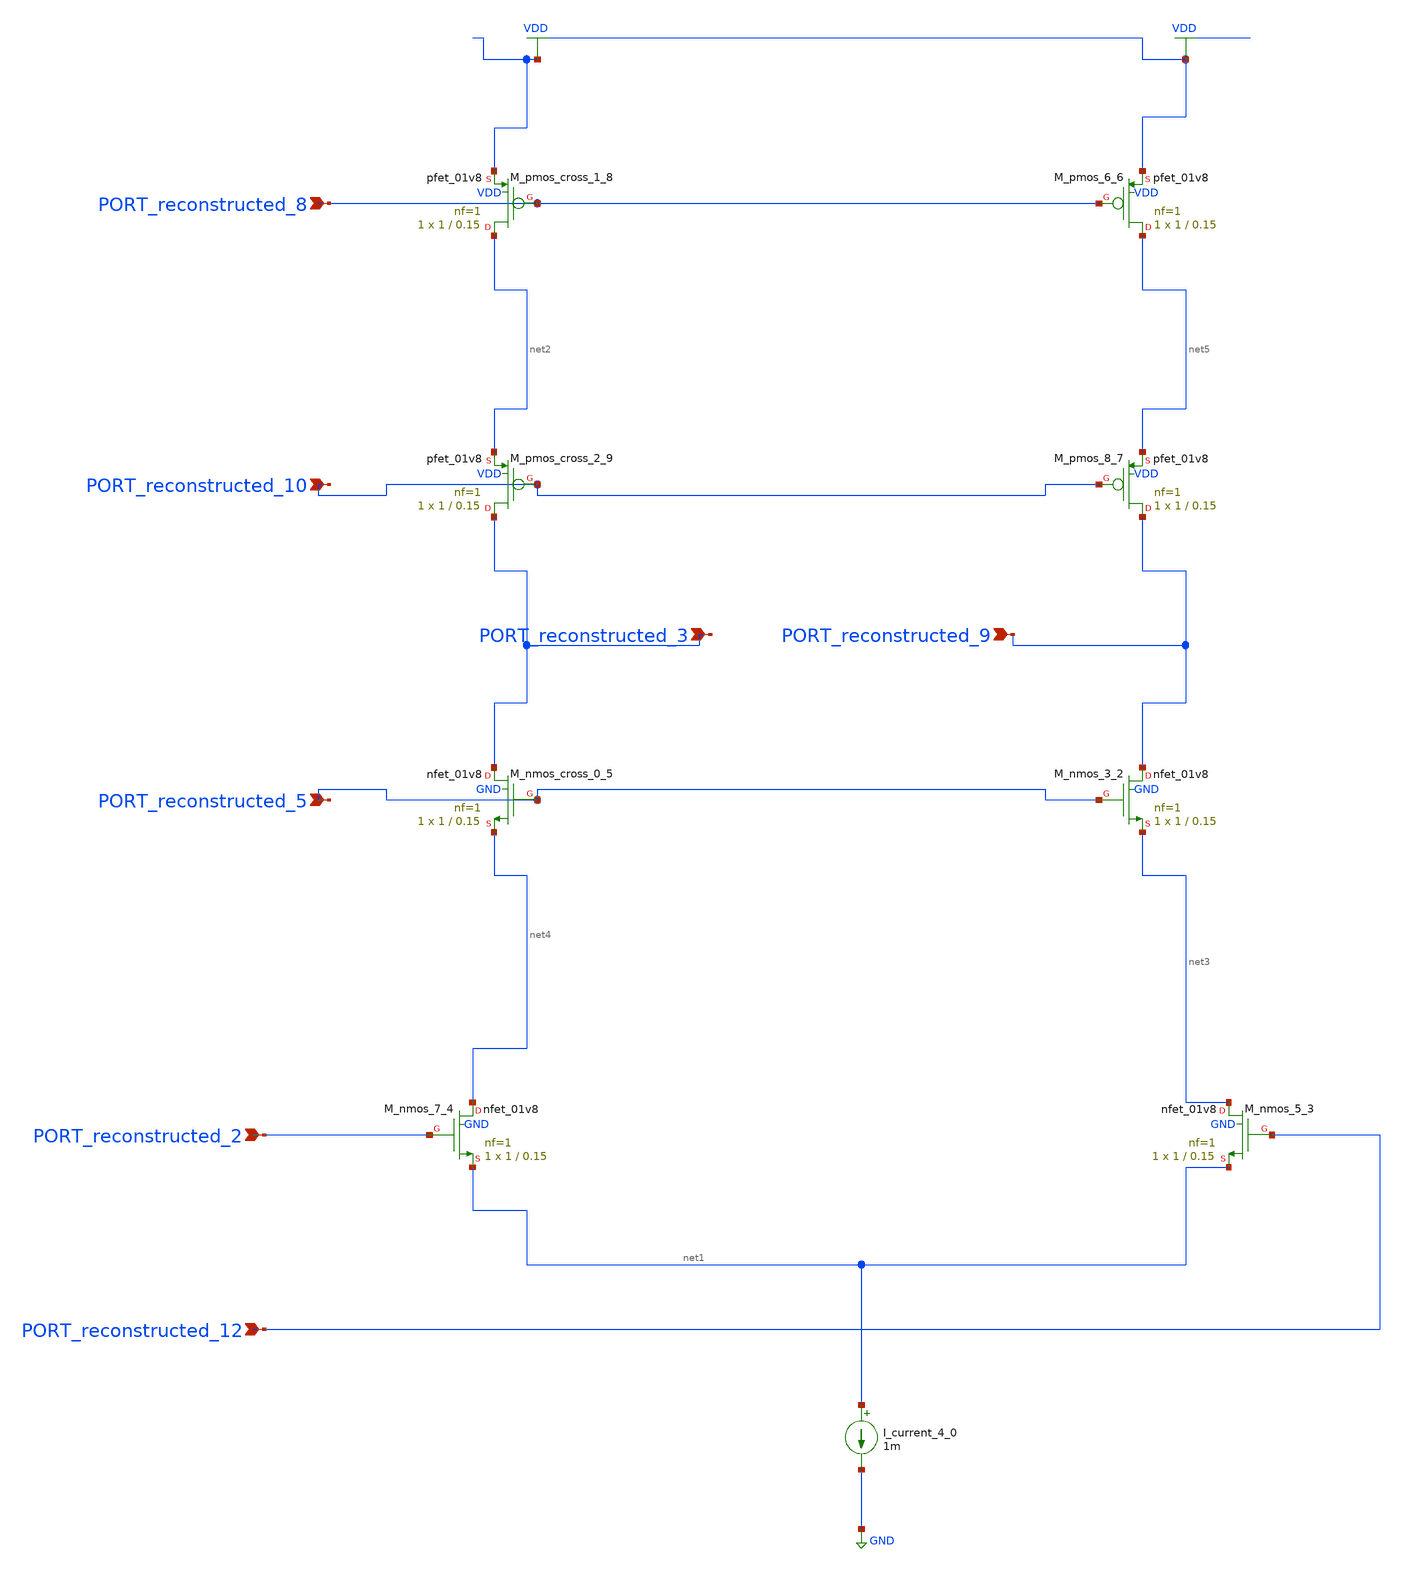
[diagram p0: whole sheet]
** sch_path: schematics/AMSNet/720.sch
**.subckt 720 PORT_reconstructed_3 PORT_reconstructed_5 PORT_reconstructed_10 PORT_reconstructed_2
*+ PORT_reconstructed_9 PORT_reconstructed_8 PORT_reconstructed_12
*.ipin PORT_reconstructed_3
*.ipin PORT_reconstructed_5
*.ipin PORT_reconstructed_10
*.ipin PORT_reconstructed_2
*.ipin PORT_reconstructed_9
*.ipin PORT_reconstructed_8
*.ipin PORT_reconstructed_12
I_current_4_0 net1 GND 1m
XM_nmos_3_2 PORT_reconstructed_9 PORT_reconstructed_5 net3 GND sky130_fd_pr__nfet_01v8 L=0.15 W=1 nf=1
+ ad='int((1 + 1)/2) * 1 / 1 * 0.29' as='int((1 + 2)/2) * 1 / 1 * 0.29' pd='2*int((1 + 1)/2) * (1 / 1 + 0.29)'
+ ps='2*int((1 + 2)/2) * (1 / 1 + 0.29)' nrd='0.29 / 1 ' nrs='0.29 / 1 ' sa=0 sb=0 sd=0 mult=1 m=1
XM_nmos_5_3 net3 PORT_reconstructed_12 net1 GND sky130_fd_pr__nfet_01v8 L=0.15 W=1 nf=1 ad='int((1 + 1)/2) * 1 / 1 * 0.29'
+ as='int((1 + 2)/2) * 1 / 1 * 0.29' pd='2*int((1 + 1)/2) * (1 / 1 + 0.29)' ps='2*int((1 + 2)/2) * (1 / 1 + 0.29)'
+ nrd='0.29 / 1 ' nrs='0.29 / 1 ' sa=0 sb=0 sd=0 mult=1 m=1
XM_nmos_7_4 net4 PORT_reconstructed_2 net1 GND sky130_fd_pr__nfet_01v8 L=0.15 W=1 nf=1 ad='int((1 + 1)/2) * 1 / 1 * 0.29'
+ as='int((1 + 2)/2) * 1 / 1 * 0.29' pd='2*int((1 + 1)/2) * (1 / 1 + 0.29)' ps='2*int((1 + 2)/2) * (1 / 1 + 0.29)'
+ nrd='0.29 / 1 ' nrs='0.29 / 1 ' sa=0 sb=0 sd=0 mult=1 m=1
XM_nmos_cross_0_5 PORT_reconstructed_3 PORT_reconstructed_5 net4 GND sky130_fd_pr__nfet_01v8 L=0.15 W=1
+ nf=1 ad='int((1 + 1)/2) * 1 / 1 * 0.29' as='int((1 + 2)/2) * 1 / 1 * 0.29' pd='2*int((1 + 1)/2) * (1 / 1 + 0.29)'
+ ps='2*int((1 + 2)/2) * (1 / 1 + 0.29)' nrd='0.29 / 1 ' nrs='0.29 / 1 ' sa=0 sb=0 sd=0 mult=1 m=1
XM_pmos_6_6 net5 PORT_reconstructed_8 VDD VDD sky130_fd_pr__pfet_01v8 L=0.15 W=1 nf=1 ad='int((1 + 1)/2) * 1 / 1 * 0.29'
+ as='int((1 + 2)/2) * 1 / 1 * 0.29' pd='2*int((1 + 1)/2) * (1 / 1 + 0.29)' ps='2*int((1 + 2)/2) * (1 / 1 + 0.29)'
+ nrd='0.29 / 1 ' nrs='0.29 / 1 ' sa=0 sb=0 sd=0 mult=1 m=1
XM_pmos_8_7 PORT_reconstructed_9 PORT_reconstructed_10 net5 VDD sky130_fd_pr__pfet_01v8 L=0.15 W=1 nf=1
+ ad='int((1 + 1)/2) * 1 / 1 * 0.29' as='int((1 + 2)/2) * 1 / 1 * 0.29' pd='2*int((1 + 1)/2) * (1 / 1 + 0.29)'
+ ps='2*int((1 + 2)/2) * (1 / 1 + 0.29)' nrd='0.29 / 1 ' nrs='0.29 / 1 ' sa=0 sb=0 sd=0 mult=1 m=1
XM_pmos_cross_1_8 net2 PORT_reconstructed_8 VDD VDD sky130_fd_pr__pfet_01v8 L=0.15 W=1 nf=1 ad='int((1 + 1)/2) * 1 / 1 * 0.29'
+ as='int((1 + 2)/2) * 1 / 1 * 0.29' pd='2*int((1 + 1)/2) * (1 / 1 + 0.29)' ps='2*int((1 + 2)/2) * (1 / 1 + 0.29)'
+ nrd='0.29 / 1 ' nrs='0.29 / 1 ' sa=0 sb=0 sd=0 mult=1 m=1
XM_pmos_cross_2_9 PORT_reconstructed_3 PORT_reconstructed_10 net2 VDD sky130_fd_pr__pfet_01v8 L=0.15
+ W=1 nf=1 ad='int((1 + 1)/2) * 1 / 1 * 0.29' as='int((1 + 2)/2) * 1 / 1 * 0.29' pd='2*int((1 + 1)/2) * (1 / 1 + 0.29)'
+ ps='2*int((1 + 2)/2) * (1 / 1 + 0.29)' nrd='0.29 / 1 ' nrs='0.29 / 1 ' sa=0 sb=0 sd=0 mult=1 m=1
**.ends
.GLOBAL GND
.GLOBAL VDD
.end
